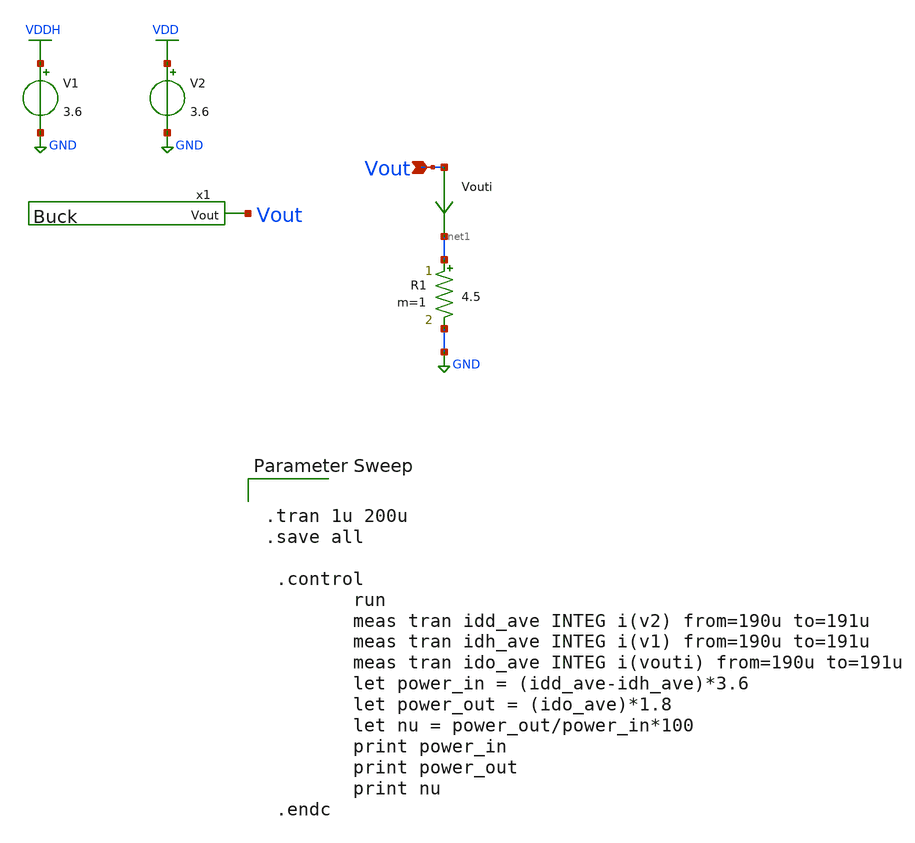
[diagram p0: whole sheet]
** sch_path: Ene_Thompson/test_Buck.sch
**.subckt test_Buck Vout
*.ipin Vout
x1 Vout Buck
V1 VDDH GND 3.6
R1 net1 GND 4.5 m=1
V2 VDD GND 3.6
Vouti Vout net1 0
.save i(vouti)
**** begin user architecture code

.lib $::SKYWATER_MODELS/sky130.lib.spice tt


.tran 1u 200u
.save all

 .control
        run
        meas tran idd_ave INTEG i(v2) from=190u to=191u
        meas tran idh_ave INTEG i(v1) from=190u to=191u
        meas tran ido_ave INTEG i(vouti) from=190u to=191u
        let power_in = (idd_ave-idh_ave)*3.6
        let power_out = (ido_ave)*1.8
        let nu = power_out/power_in*100
        print power_in
        print power_out
        print nu
 .endc


**** end user architecture code
**.ends

* expanding   symbol:  Buck.sym # of pins=1
** sym_path: Ene_Thompson/Buck.sym
** sch_path: Ene_Thompson/Buck.sch
.subckt Buck Vout
*.opin Vout
XM1 vl pswitch VDD VDD sky130_fd_pr__pfet_g5v0d10v5 L=0.5 W=20 nf=1 ad='int((nf+1)/2) * W/nf * 0.29'
+ as='int((nf+2)/2) * W/nf * 0.29' pd='2*int((nf+1)/2) * (W/nf + 0.29)' ps='2*int((nf+2)/2) * (W/nf + 0.29)'
+ nrd='0.29 / W' nrs='0.29 / W' sa=0 sb=0 sd=0 mult=1000 m=1000
XM2 vl nswitch GND GND sky130_fd_pr__nfet_g5v0d10v5 L=0.5 W=20 nf=1 ad='int((nf+1)/2) * W/nf * 0.29'
+ as='int((nf+2)/2) * W/nf * 0.29' pd='2*int((nf+1)/2) * (W/nf + 0.29)' ps='2*int((nf+2)/2) * (W/nf + 0.29)'
+ nrd='0.29 / W' nrs='0.29 / W' sa=0 sb=0 sd=0 mult=1000 m=1000
L1 net2 Vout 4.7u m=1
C1 Vout net1 1u m=1
V1 pswitch GND PULSE(0 5 0 0.01u 0.01u 0.5u 1u)
R1 vl net2 1.5m m=1
R2 GND net1 10m m=1
V2 nswitch GND PULSE(0 5 50n 0.01u 0.01u 0.55u 1u)
.ends

.GLOBAL VDDH
.GLOBAL GND
.GLOBAL VDD
.end
